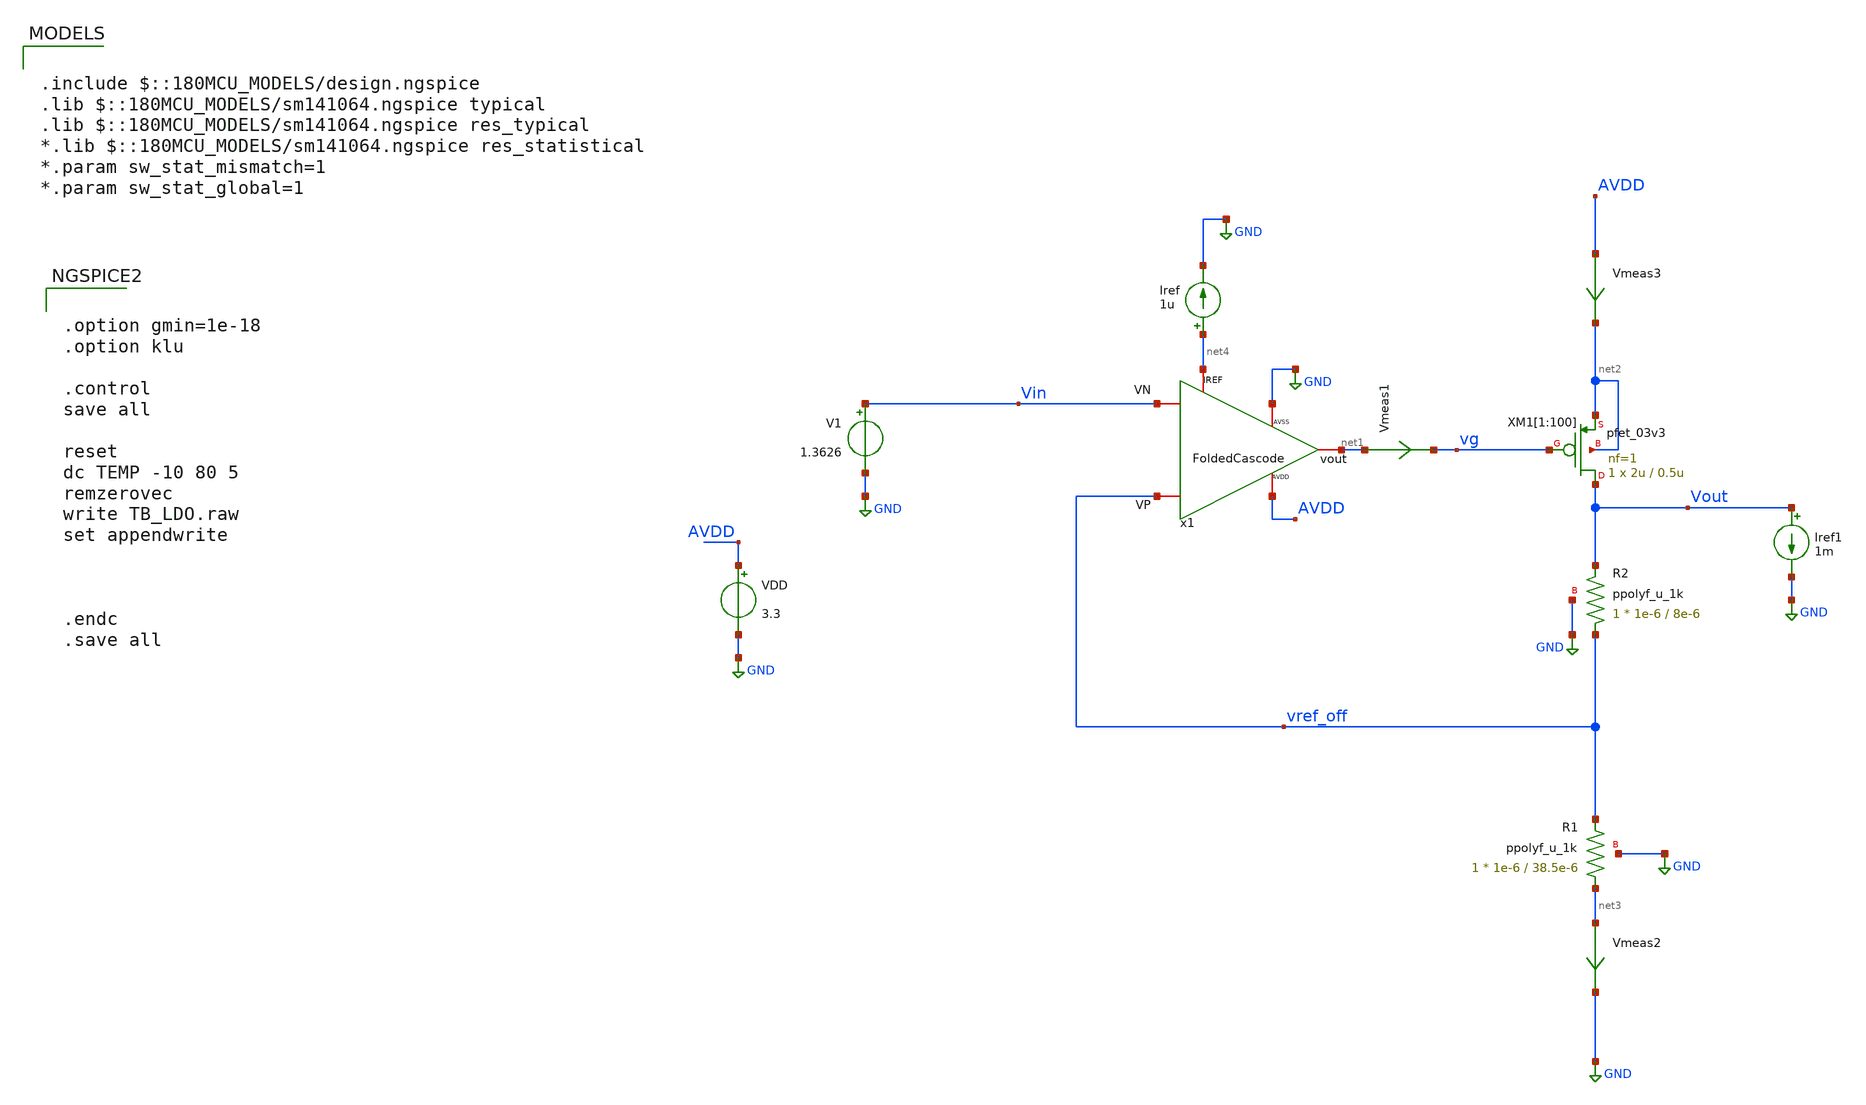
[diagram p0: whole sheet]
** sch_path: Voltage_Reference/LDO/TB_LDO.sch
**.subckt TB_LDO
VDD AVDD GND 3.3
Iref net4 GND 1u
Vmeas2 net3 GND 0
.save i(vmeas2)
V1 Vin GND 1.3626
XM1[1] Vout vg net2 net2 pfet_03v3 L=0.5u W=2u nf=1 ad='int((nf+1)/2) * W/nf * 0.18u' as='int((nf+2)/2) * W/nf * 0.18u'
+ pd='2*int((nf+1)/2) * (W/nf + 0.18u)' ps='2*int((nf+2)/2) * (W/nf + 0.18u)' nrd='0.18u / W' nrs='0.18u / W'
+ sa=0 sb=0 sd=0 m=1
XM1[2] Vout vg net2 net2 pfet_03v3 L=0.5u W=2u nf=1 ad='int((nf+1)/2) * W/nf * 0.18u' as='int((nf+2)/2) * W/nf * 0.18u'
+ pd='2*int((nf+1)/2) * (W/nf + 0.18u)' ps='2*int((nf+2)/2) * (W/nf + 0.18u)' nrd='0.18u / W' nrs='0.18u / W'
+ sa=0 sb=0 sd=0 m=1
XM1[3] Vout vg net2 net2 pfet_03v3 L=0.5u W=2u nf=1 ad='int((nf+1)/2) * W/nf * 0.18u' as='int((nf+2)/2) * W/nf * 0.18u'
+ pd='2*int((nf+1)/2) * (W/nf + 0.18u)' ps='2*int((nf+2)/2) * (W/nf + 0.18u)' nrd='0.18u / W' nrs='0.18u / W'
+ sa=0 sb=0 sd=0 m=1
XM1[4] Vout vg net2 net2 pfet_03v3 L=0.5u W=2u nf=1 ad='int((nf+1)/2) * W/nf * 0.18u' as='int((nf+2)/2) * W/nf * 0.18u'
+ pd='2*int((nf+1)/2) * (W/nf + 0.18u)' ps='2*int((nf+2)/2) * (W/nf + 0.18u)' nrd='0.18u / W' nrs='0.18u / W'
+ sa=0 sb=0 sd=0 m=1
XM1[5] Vout vg net2 net2 pfet_03v3 L=0.5u W=2u nf=1 ad='int((nf+1)/2) * W/nf * 0.18u' as='int((nf+2)/2) * W/nf * 0.18u'
+ pd='2*int((nf+1)/2) * (W/nf + 0.18u)' ps='2*int((nf+2)/2) * (W/nf + 0.18u)' nrd='0.18u / W' nrs='0.18u / W'
+ sa=0 sb=0 sd=0 m=1
XM1[6] Vout vg net2 net2 pfet_03v3 L=0.5u W=2u nf=1 ad='int((nf+1)/2) * W/nf * 0.18u' as='int((nf+2)/2) * W/nf * 0.18u'
+ pd='2*int((nf+1)/2) * (W/nf + 0.18u)' ps='2*int((nf+2)/2) * (W/nf + 0.18u)' nrd='0.18u / W' nrs='0.18u / W'
+ sa=0 sb=0 sd=0 m=1
XM1[7] Vout vg net2 net2 pfet_03v3 L=0.5u W=2u nf=1 ad='int((nf+1)/2) * W/nf * 0.18u' as='int((nf+2)/2) * W/nf * 0.18u'
+ pd='2*int((nf+1)/2) * (W/nf + 0.18u)' ps='2*int((nf+2)/2) * (W/nf + 0.18u)' nrd='0.18u / W' nrs='0.18u / W'
+ sa=0 sb=0 sd=0 m=1
XM1[8] Vout vg net2 net2 pfet_03v3 L=0.5u W=2u nf=1 ad='int((nf+1)/2) * W/nf * 0.18u' as='int((nf+2)/2) * W/nf * 0.18u'
+ pd='2*int((nf+1)/2) * (W/nf + 0.18u)' ps='2*int((nf+2)/2) * (W/nf + 0.18u)' nrd='0.18u / W' nrs='0.18u / W'
+ sa=0 sb=0 sd=0 m=1
XM1[9] Vout vg net2 net2 pfet_03v3 L=0.5u W=2u nf=1 ad='int((nf+1)/2) * W/nf * 0.18u' as='int((nf+2)/2) * W/nf * 0.18u'
+ pd='2*int((nf+1)/2) * (W/nf + 0.18u)' ps='2*int((nf+2)/2) * (W/nf + 0.18u)' nrd='0.18u / W' nrs='0.18u / W'
+ sa=0 sb=0 sd=0 m=1
XM1[10] Vout vg net2 net2 pfet_03v3 L=0.5u W=2u nf=1 ad='int((nf+1)/2) * W/nf * 0.18u' as='int((nf+2)/2) * W/nf * 0.18u'
+ pd='2*int((nf+1)/2) * (W/nf + 0.18u)' ps='2*int((nf+2)/2) * (W/nf + 0.18u)' nrd='0.18u / W' nrs='0.18u / W'
+ sa=0 sb=0 sd=0 m=1
XM1[11] Vout vg net2 net2 pfet_03v3 L=0.5u W=2u nf=1 ad='int((nf+1)/2) * W/nf * 0.18u' as='int((nf+2)/2) * W/nf * 0.18u'
+ pd='2*int((nf+1)/2) * (W/nf + 0.18u)' ps='2*int((nf+2)/2) * (W/nf + 0.18u)' nrd='0.18u / W' nrs='0.18u / W'
+ sa=0 sb=0 sd=0 m=1
XM1[12] Vout vg net2 net2 pfet_03v3 L=0.5u W=2u nf=1 ad='int((nf+1)/2) * W/nf * 0.18u' as='int((nf+2)/2) * W/nf * 0.18u'
+ pd='2*int((nf+1)/2) * (W/nf + 0.18u)' ps='2*int((nf+2)/2) * (W/nf + 0.18u)' nrd='0.18u / W' nrs='0.18u / W'
+ sa=0 sb=0 sd=0 m=1
XM1[13] Vout vg net2 net2 pfet_03v3 L=0.5u W=2u nf=1 ad='int((nf+1)/2) * W/nf * 0.18u' as='int((nf+2)/2) * W/nf * 0.18u'
+ pd='2*int((nf+1)/2) * (W/nf + 0.18u)' ps='2*int((nf+2)/2) * (W/nf + 0.18u)' nrd='0.18u / W' nrs='0.18u / W'
+ sa=0 sb=0 sd=0 m=1
XM1[14] Vout vg net2 net2 pfet_03v3 L=0.5u W=2u nf=1 ad='int((nf+1)/2) * W/nf * 0.18u' as='int((nf+2)/2) * W/nf * 0.18u'
+ pd='2*int((nf+1)/2) * (W/nf + 0.18u)' ps='2*int((nf+2)/2) * (W/nf + 0.18u)' nrd='0.18u / W' nrs='0.18u / W'
+ sa=0 sb=0 sd=0 m=1
XM1[15] Vout vg net2 net2 pfet_03v3 L=0.5u W=2u nf=1 ad='int((nf+1)/2) * W/nf * 0.18u' as='int((nf+2)/2) * W/nf * 0.18u'
+ pd='2*int((nf+1)/2) * (W/nf + 0.18u)' ps='2*int((nf+2)/2) * (W/nf + 0.18u)' nrd='0.18u / W' nrs='0.18u / W'
+ sa=0 sb=0 sd=0 m=1
XM1[16] Vout vg net2 net2 pfet_03v3 L=0.5u W=2u nf=1 ad='int((nf+1)/2) * W/nf * 0.18u' as='int((nf+2)/2) * W/nf * 0.18u'
+ pd='2*int((nf+1)/2) * (W/nf + 0.18u)' ps='2*int((nf+2)/2) * (W/nf + 0.18u)' nrd='0.18u / W' nrs='0.18u / W'
+ sa=0 sb=0 sd=0 m=1
XM1[17] Vout vg net2 net2 pfet_03v3 L=0.5u W=2u nf=1 ad='int((nf+1)/2) * W/nf * 0.18u' as='int((nf+2)/2) * W/nf * 0.18u'
+ pd='2*int((nf+1)/2) * (W/nf + 0.18u)' ps='2*int((nf+2)/2) * (W/nf + 0.18u)' nrd='0.18u / W' nrs='0.18u / W'
+ sa=0 sb=0 sd=0 m=1
XM1[18] Vout vg net2 net2 pfet_03v3 L=0.5u W=2u nf=1 ad='int((nf+1)/2) * W/nf * 0.18u' as='int((nf+2)/2) * W/nf * 0.18u'
+ pd='2*int((nf+1)/2) * (W/nf + 0.18u)' ps='2*int((nf+2)/2) * (W/nf + 0.18u)' nrd='0.18u / W' nrs='0.18u / W'
+ sa=0 sb=0 sd=0 m=1
XM1[19] Vout vg net2 net2 pfet_03v3 L=0.5u W=2u nf=1 ad='int((nf+1)/2) * W/nf * 0.18u' as='int((nf+2)/2) * W/nf * 0.18u'
+ pd='2*int((nf+1)/2) * (W/nf + 0.18u)' ps='2*int((nf+2)/2) * (W/nf + 0.18u)' nrd='0.18u / W' nrs='0.18u / W'
+ sa=0 sb=0 sd=0 m=1
XM1[20] Vout vg net2 net2 pfet_03v3 L=0.5u W=2u nf=1 ad='int((nf+1)/2) * W/nf * 0.18u' as='int((nf+2)/2) * W/nf * 0.18u'
+ pd='2*int((nf+1)/2) * (W/nf + 0.18u)' ps='2*int((nf+2)/2) * (W/nf + 0.18u)' nrd='0.18u / W' nrs='0.18u / W'
+ sa=0 sb=0 sd=0 m=1
XM1[21] Vout vg net2 net2 pfet_03v3 L=0.5u W=2u nf=1 ad='int((nf+1)/2) * W/nf * 0.18u' as='int((nf+2)/2) * W/nf * 0.18u'
+ pd='2*int((nf+1)/2) * (W/nf + 0.18u)' ps='2*int((nf+2)/2) * (W/nf + 0.18u)' nrd='0.18u / W' nrs='0.18u / W'
+ sa=0 sb=0 sd=0 m=1
XM1[22] Vout vg net2 net2 pfet_03v3 L=0.5u W=2u nf=1 ad='int((nf+1)/2) * W/nf * 0.18u' as='int((nf+2)/2) * W/nf * 0.18u'
+ pd='2*int((nf+1)/2) * (W/nf + 0.18u)' ps='2*int((nf+2)/2) * (W/nf + 0.18u)' nrd='0.18u / W' nrs='0.18u / W'
+ sa=0 sb=0 sd=0 m=1
XM1[23] Vout vg net2 net2 pfet_03v3 L=0.5u W=2u nf=1 ad='int((nf+1)/2) * W/nf * 0.18u' as='int((nf+2)/2) * W/nf * 0.18u'
+ pd='2*int((nf+1)/2) * (W/nf + 0.18u)' ps='2*int((nf+2)/2) * (W/nf + 0.18u)' nrd='0.18u / W' nrs='0.18u / W'
+ sa=0 sb=0 sd=0 m=1
XM1[24] Vout vg net2 net2 pfet_03v3 L=0.5u W=2u nf=1 ad='int((nf+1)/2) * W/nf * 0.18u' as='int((nf+2)/2) * W/nf * 0.18u'
+ pd='2*int((nf+1)/2) * (W/nf + 0.18u)' ps='2*int((nf+2)/2) * (W/nf + 0.18u)' nrd='0.18u / W' nrs='0.18u / W'
+ sa=0 sb=0 sd=0 m=1
XM1[25] Vout vg net2 net2 pfet_03v3 L=0.5u W=2u nf=1 ad='int((nf+1)/2) * W/nf * 0.18u' as='int((nf+2)/2) * W/nf * 0.18u'
+ pd='2*int((nf+1)/2) * (W/nf + 0.18u)' ps='2*int((nf+2)/2) * (W/nf + 0.18u)' nrd='0.18u / W' nrs='0.18u / W'
+ sa=0 sb=0 sd=0 m=1
XM1[26] Vout vg net2 net2 pfet_03v3 L=0.5u W=2u nf=1 ad='int((nf+1)/2) * W/nf * 0.18u' as='int((nf+2)/2) * W/nf * 0.18u'
+ pd='2*int((nf+1)/2) * (W/nf + 0.18u)' ps='2*int((nf+2)/2) * (W/nf + 0.18u)' nrd='0.18u / W' nrs='0.18u / W'
+ sa=0 sb=0 sd=0 m=1
XM1[27] Vout vg net2 net2 pfet_03v3 L=0.5u W=2u nf=1 ad='int((nf+1)/2) * W/nf * 0.18u' as='int((nf+2)/2) * W/nf * 0.18u'
+ pd='2*int((nf+1)/2) * (W/nf + 0.18u)' ps='2*int((nf+2)/2) * (W/nf + 0.18u)' nrd='0.18u / W' nrs='0.18u / W'
+ sa=0 sb=0 sd=0 m=1
XM1[28] Vout vg net2 net2 pfet_03v3 L=0.5u W=2u nf=1 ad='int((nf+1)/2) * W/nf * 0.18u' as='int((nf+2)/2) * W/nf * 0.18u'
+ pd='2*int((nf+1)/2) * (W/nf + 0.18u)' ps='2*int((nf+2)/2) * (W/nf + 0.18u)' nrd='0.18u / W' nrs='0.18u / W'
+ sa=0 sb=0 sd=0 m=1
XM1[29] Vout vg net2 net2 pfet_03v3 L=0.5u W=2u nf=1 ad='int((nf+1)/2) * W/nf * 0.18u' as='int((nf+2)/2) * W/nf * 0.18u'
+ pd='2*int((nf+1)/2) * (W/nf + 0.18u)' ps='2*int((nf+2)/2) * (W/nf + 0.18u)' nrd='0.18u / W' nrs='0.18u / W'
+ sa=0 sb=0 sd=0 m=1
XM1[30] Vout vg net2 net2 pfet_03v3 L=0.5u W=2u nf=1 ad='int((nf+1)/2) * W/nf * 0.18u' as='int((nf+2)/2) * W/nf * 0.18u'
+ pd='2*int((nf+1)/2) * (W/nf + 0.18u)' ps='2*int((nf+2)/2) * (W/nf + 0.18u)' nrd='0.18u / W' nrs='0.18u / W'
+ sa=0 sb=0 sd=0 m=1
XM1[31] Vout vg net2 net2 pfet_03v3 L=0.5u W=2u nf=1 ad='int((nf+1)/2) * W/nf * 0.18u' as='int((nf+2)/2) * W/nf * 0.18u'
+ pd='2*int((nf+1)/2) * (W/nf + 0.18u)' ps='2*int((nf+2)/2) * (W/nf + 0.18u)' nrd='0.18u / W' nrs='0.18u / W'
+ sa=0 sb=0 sd=0 m=1
XM1[32] Vout vg net2 net2 pfet_03v3 L=0.5u W=2u nf=1 ad='int((nf+1)/2) * W/nf * 0.18u' as='int((nf+2)/2) * W/nf * 0.18u'
+ pd='2*int((nf+1)/2) * (W/nf + 0.18u)' ps='2*int((nf+2)/2) * (W/nf + 0.18u)' nrd='0.18u / W' nrs='0.18u / W'
+ sa=0 sb=0 sd=0 m=1
XM1[33] Vout vg net2 net2 pfet_03v3 L=0.5u W=2u nf=1 ad='int((nf+1)/2) * W/nf * 0.18u' as='int((nf+2)/2) * W/nf * 0.18u'
+ pd='2*int((nf+1)/2) * (W/nf + 0.18u)' ps='2*int((nf+2)/2) * (W/nf + 0.18u)' nrd='0.18u / W' nrs='0.18u / W'
+ sa=0 sb=0 sd=0 m=1
XM1[34] Vout vg net2 net2 pfet_03v3 L=0.5u W=2u nf=1 ad='int((nf+1)/2) * W/nf * 0.18u' as='int((nf+2)/2) * W/nf * 0.18u'
+ pd='2*int((nf+1)/2) * (W/nf + 0.18u)' ps='2*int((nf+2)/2) * (W/nf + 0.18u)' nrd='0.18u / W' nrs='0.18u / W'
+ sa=0 sb=0 sd=0 m=1
XM1[35] Vout vg net2 net2 pfet_03v3 L=0.5u W=2u nf=1 ad='int((nf+1)/2) * W/nf * 0.18u' as='int((nf+2)/2) * W/nf * 0.18u'
+ pd='2*int((nf+1)/2) * (W/nf + 0.18u)' ps='2*int((nf+2)/2) * (W/nf + 0.18u)' nrd='0.18u / W' nrs='0.18u / W'
+ sa=0 sb=0 sd=0 m=1
XM1[36] Vout vg net2 net2 pfet_03v3 L=0.5u W=2u nf=1 ad='int((nf+1)/2) * W/nf * 0.18u' as='int((nf+2)/2) * W/nf * 0.18u'
+ pd='2*int((nf+1)/2) * (W/nf + 0.18u)' ps='2*int((nf+2)/2) * (W/nf + 0.18u)' nrd='0.18u / W' nrs='0.18u / W'
+ sa=0 sb=0 sd=0 m=1
XM1[37] Vout vg net2 net2 pfet_03v3 L=0.5u W=2u nf=1 ad='int((nf+1)/2) * W/nf * 0.18u' as='int((nf+2)/2) * W/nf * 0.18u'
+ pd='2*int((nf+1)/2) * (W/nf + 0.18u)' ps='2*int((nf+2)/2) * (W/nf + 0.18u)' nrd='0.18u / W' nrs='0.18u / W'
+ sa=0 sb=0 sd=0 m=1
XM1[38] Vout vg net2 net2 pfet_03v3 L=0.5u W=2u nf=1 ad='int((nf+1)/2) * W/nf * 0.18u' as='int((nf+2)/2) * W/nf * 0.18u'
+ pd='2*int((nf+1)/2) * (W/nf + 0.18u)' ps='2*int((nf+2)/2) * (W/nf + 0.18u)' nrd='0.18u / W' nrs='0.18u / W'
+ sa=0 sb=0 sd=0 m=1
XM1[39] Vout vg net2 net2 pfet_03v3 L=0.5u W=2u nf=1 ad='int((nf+1)/2) * W/nf * 0.18u' as='int((nf+2)/2) * W/nf * 0.18u'
+ pd='2*int((nf+1)/2) * (W/nf + 0.18u)' ps='2*int((nf+2)/2) * (W/nf + 0.18u)' nrd='0.18u / W' nrs='0.18u / W'
+ sa=0 sb=0 sd=0 m=1
XM1[40] Vout vg net2 net2 pfet_03v3 L=0.5u W=2u nf=1 ad='int((nf+1)/2) * W/nf * 0.18u' as='int((nf+2)/2) * W/nf * 0.18u'
+ pd='2*int((nf+1)/2) * (W/nf + 0.18u)' ps='2*int((nf+2)/2) * (W/nf + 0.18u)' nrd='0.18u / W' nrs='0.18u / W'
+ sa=0 sb=0 sd=0 m=1
XM1[41] Vout vg net2 net2 pfet_03v3 L=0.5u W=2u nf=1 ad='int((nf+1)/2) * W/nf * 0.18u' as='int((nf+2)/2) * W/nf * 0.18u'
+ pd='2*int((nf+1)/2) * (W/nf + 0.18u)' ps='2*int((nf+2)/2) * (W/nf + 0.18u)' nrd='0.18u / W' nrs='0.18u / W'
+ sa=0 sb=0 sd=0 m=1
XM1[42] Vout vg net2 net2 pfet_03v3 L=0.5u W=2u nf=1 ad='int((nf+1)/2) * W/nf * 0.18u' as='int((nf+2)/2) * W/nf * 0.18u'
+ pd='2*int((nf+1)/2) * (W/nf + 0.18u)' ps='2*int((nf+2)/2) * (W/nf + 0.18u)' nrd='0.18u / W' nrs='0.18u / W'
+ sa=0 sb=0 sd=0 m=1
XM1[43] Vout vg net2 net2 pfet_03v3 L=0.5u W=2u nf=1 ad='int((nf+1)/2) * W/nf * 0.18u' as='int((nf+2)/2) * W/nf * 0.18u'
+ pd='2*int((nf+1)/2) * (W/nf + 0.18u)' ps='2*int((nf+2)/2) * (W/nf + 0.18u)' nrd='0.18u / W' nrs='0.18u / W'
+ sa=0 sb=0 sd=0 m=1
XM1[44] Vout vg net2 net2 pfet_03v3 L=0.5u W=2u nf=1 ad='int((nf+1)/2) * W/nf * 0.18u' as='int((nf+2)/2) * W/nf * 0.18u'
+ pd='2*int((nf+1)/2) * (W/nf + 0.18u)' ps='2*int((nf+2)/2) * (W/nf + 0.18u)' nrd='0.18u / W' nrs='0.18u / W'
+ sa=0 sb=0 sd=0 m=1
XM1[45] Vout vg net2 net2 pfet_03v3 L=0.5u W=2u nf=1 ad='int((nf+1)/2) * W/nf * 0.18u' as='int((nf+2)/2) * W/nf * 0.18u'
+ pd='2*int((nf+1)/2) * (W/nf + 0.18u)' ps='2*int((nf+2)/2) * (W/nf + 0.18u)' nrd='0.18u / W' nrs='0.18u / W'
+ sa=0 sb=0 sd=0 m=1
XM1[46] Vout vg net2 net2 pfet_03v3 L=0.5u W=2u nf=1 ad='int((nf+1)/2) * W/nf * 0.18u' as='int((nf+2)/2) * W/nf * 0.18u'
+ pd='2*int((nf+1)/2) * (W/nf + 0.18u)' ps='2*int((nf+2)/2) * (W/nf + 0.18u)' nrd='0.18u / W' nrs='0.18u / W'
+ sa=0 sb=0 sd=0 m=1
XM1[47] Vout vg net2 net2 pfet_03v3 L=0.5u W=2u nf=1 ad='int((nf+1)/2) * W/nf * 0.18u' as='int((nf+2)/2) * W/nf * 0.18u'
+ pd='2*int((nf+1)/2) * (W/nf + 0.18u)' ps='2*int((nf+2)/2) * (W/nf + 0.18u)' nrd='0.18u / W' nrs='0.18u / W'
+ sa=0 sb=0 sd=0 m=1
XM1[48] Vout vg net2 net2 pfet_03v3 L=0.5u W=2u nf=1 ad='int((nf+1)/2) * W/nf * 0.18u' as='int((nf+2)/2) * W/nf * 0.18u'
+ pd='2*int((nf+1)/2) * (W/nf + 0.18u)' ps='2*int((nf+2)/2) * (W/nf + 0.18u)' nrd='0.18u / W' nrs='0.18u / W'
+ sa=0 sb=0 sd=0 m=1
XM1[49] Vout vg net2 net2 pfet_03v3 L=0.5u W=2u nf=1 ad='int((nf+1)/2) * W/nf * 0.18u' as='int((nf+2)/2) * W/nf * 0.18u'
+ pd='2*int((nf+1)/2) * (W/nf + 0.18u)' ps='2*int((nf+2)/2) * (W/nf + 0.18u)' nrd='0.18u / W' nrs='0.18u / W'
+ sa=0 sb=0 sd=0 m=1
XM1[50] Vout vg net2 net2 pfet_03v3 L=0.5u W=2u nf=1 ad='int((nf+1)/2) * W/nf * 0.18u' as='int((nf+2)/2) * W/nf * 0.18u'
+ pd='2*int((nf+1)/2) * (W/nf + 0.18u)' ps='2*int((nf+2)/2) * (W/nf + 0.18u)' nrd='0.18u / W' nrs='0.18u / W'
+ sa=0 sb=0 sd=0 m=1
XM1[51] Vout vg net2 net2 pfet_03v3 L=0.5u W=2u nf=1 ad='int((nf+1)/2) * W/nf * 0.18u' as='int((nf+2)/2) * W/nf * 0.18u'
+ pd='2*int((nf+1)/2) * (W/nf + 0.18u)' ps='2*int((nf+2)/2) * (W/nf + 0.18u)' nrd='0.18u / W' nrs='0.18u / W'
+ sa=0 sb=0 sd=0 m=1
XM1[52] Vout vg net2 net2 pfet_03v3 L=0.5u W=2u nf=1 ad='int((nf+1)/2) * W/nf * 0.18u' as='int((nf+2)/2) * W/nf * 0.18u'
+ pd='2*int((nf+1)/2) * (W/nf + 0.18u)' ps='2*int((nf+2)/2) * (W/nf + 0.18u)' nrd='0.18u / W' nrs='0.18u / W'
+ sa=0 sb=0 sd=0 m=1
XM1[53] Vout vg net2 net2 pfet_03v3 L=0.5u W=2u nf=1 ad='int((nf+1)/2) * W/nf * 0.18u' as='int((nf+2)/2) * W/nf * 0.18u'
+ pd='2*int((nf+1)/2) * (W/nf + 0.18u)' ps='2*int((nf+2)/2) * (W/nf + 0.18u)' nrd='0.18u / W' nrs='0.18u / W'
+ sa=0 sb=0 sd=0 m=1
XM1[54] Vout vg net2 net2 pfet_03v3 L=0.5u W=2u nf=1 ad='int((nf+1)/2) * W/nf * 0.18u' as='int((nf+2)/2) * W/nf * 0.18u'
+ pd='2*int((nf+1)/2) * (W/nf + 0.18u)' ps='2*int((nf+2)/2) * (W/nf + 0.18u)' nrd='0.18u / W' nrs='0.18u / W'
+ sa=0 sb=0 sd=0 m=1
XM1[55] Vout vg net2 net2 pfet_03v3 L=0.5u W=2u nf=1 ad='int((nf+1)/2) * W/nf * 0.18u' as='int((nf+2)/2) * W/nf * 0.18u'
+ pd='2*int((nf+1)/2) * (W/nf + 0.18u)' ps='2*int((nf+2)/2) * (W/nf + 0.18u)' nrd='0.18u / W' nrs='0.18u / W'
+ sa=0 sb=0 sd=0 m=1
XM1[56] Vout vg net2 net2 pfet_03v3 L=0.5u W=2u nf=1 ad='int((nf+1)/2) * W/nf * 0.18u' as='int((nf+2)/2) * W/nf * 0.18u'
+ pd='2*int((nf+1)/2) * (W/nf + 0.18u)' ps='2*int((nf+2)/2) * (W/nf + 0.18u)' nrd='0.18u / W' nrs='0.18u / W'
+ sa=0 sb=0 sd=0 m=1
XM1[57] Vout vg net2 net2 pfet_03v3 L=0.5u W=2u nf=1 ad='int((nf+1)/2) * W/nf * 0.18u' as='int((nf+2)/2) * W/nf * 0.18u'
+ pd='2*int((nf+1)/2) * (W/nf + 0.18u)' ps='2*int((nf+2)/2) * (W/nf + 0.18u)' nrd='0.18u / W' nrs='0.18u / W'
+ sa=0 sb=0 sd=0 m=1
XM1[58] Vout vg net2 net2 pfet_03v3 L=0.5u W=2u nf=1 ad='int((nf+1)/2) * W/nf * 0.18u' as='int((nf+2)/2) * W/nf * 0.18u'
+ pd='2*int((nf+1)/2) * (W/nf + 0.18u)' ps='2*int((nf+2)/2) * (W/nf + 0.18u)' nrd='0.18u / W' nrs='0.18u / W'
+ sa=0 sb=0 sd=0 m=1
XM1[59] Vout vg net2 net2 pfet_03v3 L=0.5u W=2u nf=1 ad='int((nf+1)/2) * W/nf * 0.18u' as='int((nf+2)/2) * W/nf * 0.18u'
+ pd='2*int((nf+1)/2) * (W/nf + 0.18u)' ps='2*int((nf+2)/2) * (W/nf + 0.18u)' nrd='0.18u / W' nrs='0.18u / W'
+ sa=0 sb=0 sd=0 m=1
XM1[60] Vout vg net2 net2 pfet_03v3 L=0.5u W=2u nf=1 ad='int((nf+1)/2) * W/nf * 0.18u' as='int((nf+2)/2) * W/nf * 0.18u'
+ pd='2*int((nf+1)/2) * (W/nf + 0.18u)' ps='2*int((nf+2)/2) * (W/nf + 0.18u)' nrd='0.18u / W' nrs='0.18u / W'
+ sa=0 sb=0 sd=0 m=1
XM1[61] Vout vg net2 net2 pfet_03v3 L=0.5u W=2u nf=1 ad='int((nf+1)/2) * W/nf * 0.18u' as='int((nf+2)/2) * W/nf * 0.18u'
+ pd='2*int((nf+1)/2) * (W/nf + 0.18u)' ps='2*int((nf+2)/2) * (W/nf + 0.18u)' nrd='0.18u / W' nrs='0.18u / W'
+ sa=0 sb=0 sd=0 m=1
XM1[62] Vout vg net2 net2 pfet_03v3 L=0.5u W=2u nf=1 ad='int((nf+1)/2) * W/nf * 0.18u' as='int((nf+2)/2) * W/nf * 0.18u'
+ pd='2*int((nf+1)/2) * (W/nf + 0.18u)' ps='2*int((nf+2)/2) * (W/nf + 0.18u)' nrd='0.18u / W' nrs='0.18u / W'
+ sa=0 sb=0 sd=0 m=1
XM1[63] Vout vg net2 net2 pfet_03v3 L=0.5u W=2u nf=1 ad='int((nf+1)/2) * W/nf * 0.18u' as='int((nf+2)/2) * W/nf * 0.18u'
+ pd='2*int((nf+1)/2) * (W/nf + 0.18u)' ps='2*int((nf+2)/2) * (W/nf + 0.18u)' nrd='0.18u / W' nrs='0.18u / W'
+ sa=0 sb=0 sd=0 m=1
XM1[64] Vout vg net2 net2 pfet_03v3 L=0.5u W=2u nf=1 ad='int((nf+1)/2) * W/nf * 0.18u' as='int((nf+2)/2) * W/nf * 0.18u'
+ pd='2*int((nf+1)/2) * (W/nf + 0.18u)' ps='2*int((nf+2)/2) * (W/nf + 0.18u)' nrd='0.18u / W' nrs='0.18u / W'
+ sa=0 sb=0 sd=0 m=1
XM1[65] Vout vg net2 net2 pfet_03v3 L=0.5u W=2u nf=1 ad='int((nf+1)/2) * W/nf * 0.18u' as='int((nf+2)/2) * W/nf * 0.18u'
+ pd='2*int((nf+1)/2) * (W/nf + 0.18u)' ps='2*int((nf+2)/2) * (W/nf + 0.18u)' nrd='0.18u / W' nrs='0.18u / W'
+ sa=0 sb=0 sd=0 m=1
XM1[66] Vout vg net2 net2 pfet_03v3 L=0.5u W=2u nf=1 ad='int((nf+1)/2) * W/nf * 0.18u' as='int((nf+2)/2) * W/nf * 0.18u'
+ pd='2*int((nf+1)/2) * (W/nf + 0.18u)' ps='2*int((nf+2)/2) * (W/nf + 0.18u)' nrd='0.18u / W' nrs='0.18u / W'
+ sa=0 sb=0 sd=0 m=1
XM1[67] Vout vg net2 net2 pfet_03v3 L=0.5u W=2u nf=1 ad='int((nf+1)/2) * W/nf * 0.18u' as='int((nf+2)/2) * W/nf * 0.18u'
+ pd='2*int((nf+1)/2) * (W/nf + 0.18u)' ps='2*int((nf+2)/2) * (W/nf + 0.18u)' nrd='0.18u / W' nrs='0.18u / W'
+ sa=0 sb=0 sd=0 m=1
XM1[68] Vout vg net2 net2 pfet_03v3 L=0.5u W=2u nf=1 ad='int((nf+1)/2) * W/nf * 0.18u' as='int((nf+2)/2) * W/nf * 0.18u'
+ pd='2*int((nf+1)/2) * (W/nf + 0.18u)' ps='2*int((nf+2)/2) * (W/nf + 0.18u)' nrd='0.18u / W' nrs='0.18u / W'
+ sa=0 sb=0 sd=0 m=1
XM1[69] Vout vg net2 net2 pfet_03v3 L=0.5u W=2u nf=1 ad='int((nf+1)/2) * W/nf * 0.18u' as='int((nf+2)/2) * W/nf * 0.18u'
+ pd='2*int((nf+1)/2) * (W/nf + 0.18u)' ps='2*int((nf+2)/2) * (W/nf + 0.18u)' nrd='0.18u / W' nrs='0.18u / W'
+ sa=0 sb=0 sd=0 m=1
XM1[70] Vout vg net2 net2 pfet_03v3 L=0.5u W=2u nf=1 ad='int((nf+1)/2) * W/nf * 0.18u' as='int((nf+2)/2) * W/nf * 0.18u'
+ pd='2*int((nf+1)/2) * (W/nf + 0.18u)' ps='2*int((nf+2)/2) * (W/nf + 0.18u)' nrd='0.18u / W' nrs='0.18u / W'
+ sa=0 sb=0 sd=0 m=1
XM1[71] Vout vg net2 net2 pfet_03v3 L=0.5u W=2u nf=1 ad='int((nf+1)/2) * W/nf * 0.18u' as='int((nf+2)/2) * W/nf * 0.18u'
+ pd='2*int((nf+1)/2) * (W/nf + 0.18u)' ps='2*int((nf+2)/2) * (W/nf + 0.18u)' nrd='0.18u / W' nrs='0.18u / W'
+ sa=0 sb=0 sd=0 m=1
XM1[72] Vout vg net2 net2 pfet_03v3 L=0.5u W=2u nf=1 ad='int((nf+1)/2) * W/nf * 0.18u' as='int((nf+2)/2) * W/nf * 0.18u'
+ pd='2*int((nf+1)/2) * (W/nf + 0.18u)' ps='2*int((nf+2)/2) * (W/nf + 0.18u)' nrd='0.18u / W' nrs='0.18u / W'
+ sa=0 sb=0 sd=0 m=1
XM1[73] Vout vg net2 net2 pfet_03v3 L=0.5u W=2u nf=1 ad='int((nf+1)/2) * W/nf * 0.18u' as='int((nf+2)/2) * W/nf * 0.18u'
+ pd='2*int((nf+1)/2) * (W/nf + 0.18u)' ps='2*int((nf+2)/2) * (W/nf + 0.18u)' nrd='0.18u / W' nrs='0.18u / W'
+ sa=0 sb=0 sd=0 m=1
XM1[74] Vout vg net2 net2 pfet_03v3 L=0.5u W=2u nf=1 ad='int((nf+1)/2) * W/nf * 0.18u' as='int((nf+2)/2) * W/nf * 0.18u'
+ pd='2*int((nf+1)/2) * (W/nf + 0.18u)' ps='2*int((nf+2)/2) * (W/nf + 0.18u)' nrd='0.18u / W' nrs='0.18u / W'
+ sa=0 sb=0 sd=0 m=1
XM1[75] Vout vg net2 net2 pfet_03v3 L=0.5u W=2u nf=1 ad='int((nf+1)/2) * W/nf * 0.18u' as='int((nf+2)/2) * W/nf * 0.18u'
+ pd='2*int((nf+1)/2) * (W/nf + 0.18u)' ps='2*int((nf+2)/2) * (W/nf + 0.18u)' nrd='0.18u / W' nrs='0.18u / W'
+ sa=0 sb=0 sd=0 m=1
XM1[76] Vout vg net2 net2 pfet_03v3 L=0.5u W=2u nf=1 ad='int((nf+1)/2) * W/nf * 0.18u' as='int((nf+2)/2) * W/nf * 0.18u'
+ pd='2*int((nf+1)/2) * (W/nf + 0.18u)' ps='2*int((nf+2)/2) * (W/nf + 0.18u)' nrd='0.18u / W' nrs='0.18u / W'
+ sa=0 sb=0 sd=0 m=1
XM1[77] Vout vg net2 net2 pfet_03v3 L=0.5u W=2u nf=1 ad='int((nf+1)/2) * W/nf * 0.18u' as='int((nf+2)/2) * W/nf * 0.18u'
+ pd='2*int((nf+1)/2) * (W/nf + 0.18u)' ps='2*int((nf+2)/2) * (W/nf + 0.18u)' nrd='0.18u / W' nrs='0.18u / W'
+ sa=0 sb=0 sd=0 m=1
XM1[78] Vout vg net2 net2 pfet_03v3 L=0.5u W=2u nf=1 ad='int((nf+1)/2) * W/nf * 0.18u' as='int((nf+2)/2) * W/nf * 0.18u'
+ pd='2*int((nf+1)/2) * (W/nf + 0.18u)' ps='2*int((nf+2)/2) * (W/nf + 0.18u)' nrd='0.18u / W' nrs='0.18u / W'
+ sa=0 sb=0 sd=0 m=1
XM1[79] Vout vg net2 net2 pfet_03v3 L=0.5u W=2u nf=1 ad='int((nf+1)/2) * W/nf * 0.18u' as='int((nf+2)/2) * W/nf * 0.18u'
+ pd='2*int((nf+1)/2) * (W/nf + 0.18u)' ps='2*int((nf+2)/2) * (W/nf + 0.18u)' nrd='0.18u / W' nrs='0.18u / W'
+ sa=0 sb=0 sd=0 m=1
XM1[80] Vout vg net2 net2 pfet_03v3 L=0.5u W=2u nf=1 ad='int((nf+1)/2) * W/nf * 0.18u' as='int((nf+2)/2) * W/nf * 0.18u'
+ pd='2*int((nf+1)/2) * (W/nf + 0.18u)' ps='2*int((nf+2)/2) * (W/nf + 0.18u)' nrd='0.18u / W' nrs='0.18u / W'
+ sa=0 sb=0 sd=0 m=1
XM1[81] Vout vg net2 net2 pfet_03v3 L=0.5u W=2u nf=1 ad='int((nf+1)/2) * W/nf * 0.18u' as='int((nf+2)/2) * W/nf * 0.18u'
+ pd='2*int((nf+1)/2) * (W/nf + 0.18u)' ps='2*int((nf+2)/2) * (W/nf + 0.18u)' nrd='0.18u / W' nrs='0.18u / W'
+ sa=0 sb=0 sd=0 m=1
XM1[82] Vout vg net2 net2 pfet_03v3 L=0.5u W=2u nf=1 ad='int((nf+1)/2) * W/nf * 0.18u' as='int((nf+2)/2) * W/nf * 0.18u'
+ pd='2*int((nf+1)/2) * (W/nf + 0.18u)' ps='2*int((nf+2)/2) * (W/nf + 0.18u)' nrd='0.18u / W' nrs='0.18u / W'
+ sa=0 sb=0 sd=0 m=1
XM1[83] Vout vg net2 net2 pfet_03v3 L=0.5u W=2u nf=1 ad='int((nf+1)/2) * W/nf * 0.18u' as='int((nf+2)/2) * W/nf * 0.18u'
+ pd='2*int((nf+1)/2) * (W/nf + 0.18u)' ps='2*int((nf+2)/2) * (W/nf + 0.18u)' nrd='0.18u / W' nrs='0.18u / W'
+ sa=0 sb=0 sd=0 m=1
XM1[84] Vout vg net2 net2 pfet_03v3 L=0.5u W=2u nf=1 ad='int((nf+1)/2) * W/nf * 0.18u' as='int((nf+2)/2) * W/nf * 0.18u'
+ pd='2*int((nf+1)/2) * (W/nf + 0.18u)' ps='2*int((nf+2)/2) * (W/nf + 0.18u)' nrd='0.18u / W' nrs='0.18u / W'
+ sa=0 sb=0 sd=0 m=1
XM1[85] Vout vg net2 net2 pfet_03v3 L=0.5u W=2u nf=1 ad='int((nf+1)/2) * W/nf * 0.18u' as='int((nf+2)/2) * W/nf * 0.18u'
+ pd='2*int((nf+1)/2) * (W/nf + 0.18u)' ps='2*int((nf+2)/2) * (W/nf + 0.18u)' nrd='0.18u / W' nrs='0.18u / W'
+ sa=0 sb=0 sd=0 m=1
XM1[86] Vout vg net2 net2 pfet_03v3 L=0.5u W=2u nf=1 ad='int((nf+1)/2) * W/nf * 0.18u' as='int((nf+2)/2) * W/nf * 0.18u'
+ pd='2*int((nf+1)/2) * (W/nf + 0.18u)' ps='2*int((nf+2)/2) * (W/nf + 0.18u)' nrd='0.18u / W' nrs='0.18u / W'
+ sa=0 sb=0 sd=0 m=1
XM1[87] Vout vg net2 net2 pfet_03v3 L=0.5u W=2u nf=1 ad='int((nf+1)/2) * W/nf * 0.18u' as='int((nf+2)/2) * W/nf * 0.18u'
+ pd='2*int((nf+1)/2) * (W/nf + 0.18u)' ps='2*int((nf+2)/2) * (W/nf + 0.18u)' nrd='0.18u / W' nrs='0.18u / W'
+ sa=0 sb=0 sd=0 m=1
XM1[88] Vout vg net2 net2 pfet_03v3 L=0.5u W=2u nf=1 ad='int((nf+1)/2) * W/nf * 0.18u' as='int((nf+2)/2) * W/nf * 0.18u'
+ pd='2*int((nf+1)/2) * (W/nf + 0.18u)' ps='2*int((nf+2)/2) * (W/nf + 0.18u)' nrd='0.18u / W' nrs='0.18u / W'
+ sa=0 sb=0 sd=0 m=1
XM1[89] Vout vg net2 net2 pfet_03v3 L=0.5u W=2u nf=1 ad='int((nf+1)/2) * W/nf * 0.18u' as='int((nf+2)/2) * W/nf * 0.18u'
+ pd='2*int((nf+1)/2) * (W/nf + 0.18u)' ps='2*int((nf+2)/2) * (W/nf + 0.18u)' nrd='0.18u / W' nrs='0.18u / W'
+ sa=0 sb=0 sd=0 m=1
XM1[90] Vout vg net2 net2 pfet_03v3 L=0.5u W=2u nf=1 ad='int((nf+1)/2) * W/nf * 0.18u' as='int((nf+2)/2) * W/nf * 0.18u'
+ pd='2*int((nf+1)/2) * (W/nf + 0.18u)' ps='2*int((nf+2)/2) * (W/nf + 0.18u)' nrd='0.18u / W' nrs='0.18u / W'
+ sa=0 sb=0 sd=0 m=1
XM1[91] Vout vg net2 net2 pfet_03v3 L=0.5u W=2u nf=1 ad='int((nf+1)/2) * W/nf * 0.18u' as='int((nf+2)/2) * W/nf * 0.18u'
+ pd='2*int((nf+1)/2) * (W/nf + 0.18u)' ps='2*int((nf+2)/2) * (W/nf + 0.18u)' nrd='0.18u / W' nrs='0.18u / W'
+ sa=0 sb=0 sd=0 m=1
XM1[92] Vout vg net2 net2 pfet_03v3 L=0.5u W=2u nf=1 ad='int((nf+1)/2) * W/nf * 0.18u' as='int((nf+2)/2) * W/nf * 0.18u'
+ pd='2*int((nf+1)/2) * (W/nf + 0.18u)' ps='2*int((nf+2)/2) * (W/nf + 0.18u)' nrd='0.18u / W' nrs='0.18u / W'
+ sa=0 sb=0 sd=0 m=1
XM1[93] Vout vg net2 net2 pfet_03v3 L=0.5u W=2u nf=1 ad='int((nf+1)/2) * W/nf * 0.18u' as='int((nf+2)/2) * W/nf * 0.18u'
+ pd='2*int((nf+1)/2) * (W/nf + 0.18u)' ps='2*int((nf+2)/2) * (W/nf + 0.18u)' nrd='0.18u / W' nrs='0.18u / W'
+ sa=0 sb=0 sd=0 m=1
XM1[94] Vout vg net2 net2 pfet_03v3 L=0.5u W=2u nf=1 ad='int((nf+1)/2) * W/nf * 0.18u' as='int((nf+2)/2) * W/nf * 0.18u'
+ pd='2*int((nf+1)/2) * (W/nf + 0.18u)' ps='2*int((nf+2)/2) * (W/nf + 0.18u)' nrd='0.18u / W' nrs='0.18u / W'
+ sa=0 sb=0 sd=0 m=1
XM1[95] Vout vg net2 net2 pfet_03v3 L=0.5u W=2u nf=1 ad='int((nf+1)/2) * W/nf * 0.18u' as='int((nf+2)/2) * W/nf * 0.18u'
+ pd='2*int((nf+1)/2) * (W/nf + 0.18u)' ps='2*int((nf+2)/2) * (W/nf + 0.18u)' nrd='0.18u / W' nrs='0.18u / W'
+ sa=0 sb=0 sd=0 m=1
XM1[96] Vout vg net2 net2 pfet_03v3 L=0.5u W=2u nf=1 ad='int((nf+1)/2) * W/nf * 0.18u' as='int((nf+2)/2) * W/nf * 0.18u'
+ pd='2*int((nf+1)/2) * (W/nf + 0.18u)' ps='2*int((nf+2)/2) * (W/nf + 0.18u)' nrd='0.18u / W' nrs='0.18u / W'
+ sa=0 sb=0 sd=0 m=1
XM1[97] Vout vg net2 net2 pfet_03v3 L=0.5u W=2u nf=1 ad='int((nf+1)/2) * W/nf * 0.18u' as='int((nf+2)/2) * W/nf * 0.18u'
+ pd='2*int((nf+1)/2) * (W/nf + 0.18u)' ps='2*int((nf+2)/2) * (W/nf + 0.18u)' nrd='0.18u / W' nrs='0.18u / W'
+ sa=0 sb=0 sd=0 m=1
XM1[98] Vout vg net2 net2 pfet_03v3 L=0.5u W=2u nf=1 ad='int((nf+1)/2) * W/nf * 0.18u' as='int((nf+2)/2) * W/nf * 0.18u'
+ pd='2*int((nf+1)/2) * (W/nf + 0.18u)' ps='2*int((nf+2)/2) * (W/nf + 0.18u)' nrd='0.18u / W' nrs='0.18u / W'
+ sa=0 sb=0 sd=0 m=1
XM1[99] Vout vg net2 net2 pfet_03v3 L=0.5u W=2u nf=1 ad='int((nf+1)/2) * W/nf * 0.18u' as='int((nf+2)/2) * W/nf * 0.18u'
+ pd='2*int((nf+1)/2) * (W/nf + 0.18u)' ps='2*int((nf+2)/2) * (W/nf + 0.18u)' nrd='0.18u / W' nrs='0.18u / W'
+ sa=0 sb=0 sd=0 m=1
XM1[100] Vout vg net2 net2 pfet_03v3 L=0.5u W=2u nf=1 ad='int((nf+1)/2) * W/nf * 0.18u' as='int((nf+2)/2) * W/nf * 0.18u'
+ pd='2*int((nf+1)/2) * (W/nf + 0.18u)' ps='2*int((nf+2)/2) * (W/nf + 0.18u)' nrd='0.18u / W' nrs='0.18u / W'
+ sa=0 sb=0 sd=0 m=1
Vmeas1 net1 vg 0
.save i(vmeas1)
Iref1 Vout GND 1m
Vmeas3 AVDD net2 0
.save i(vmeas3)
x1 vref_off Vin net1 net4 AVDD GND FoldedCascode
XR1 net3 vref_off GND ppolyf_u_1k r_width=1e-6 r_length=38.5e-6 m=1
XR2 vref_off Vout GND ppolyf_u_1k r_width=1e-6 r_length=8e-6 m=1
**** begin user architecture code

.include $::180MCU_MODELS/design.ngspice
.lib $::180MCU_MODELS/sm141064.ngspice typical
.lib $::180MCU_MODELS/sm141064.ngspice res_typical
*.lib $::180MCU_MODELS/sm141064.ngspice res_statistical
*.param sw_stat_mismatch=1
*.param sw_stat_global=1



.option gmin=1e-18
.option klu

.control
save all

reset
dc TEMP -10 80 5
remzerovec
write TB_LDO.raw
set appendwrite



.endc
.save all


**** end user architecture code
**.ends
.GLOBAL GND
.end
